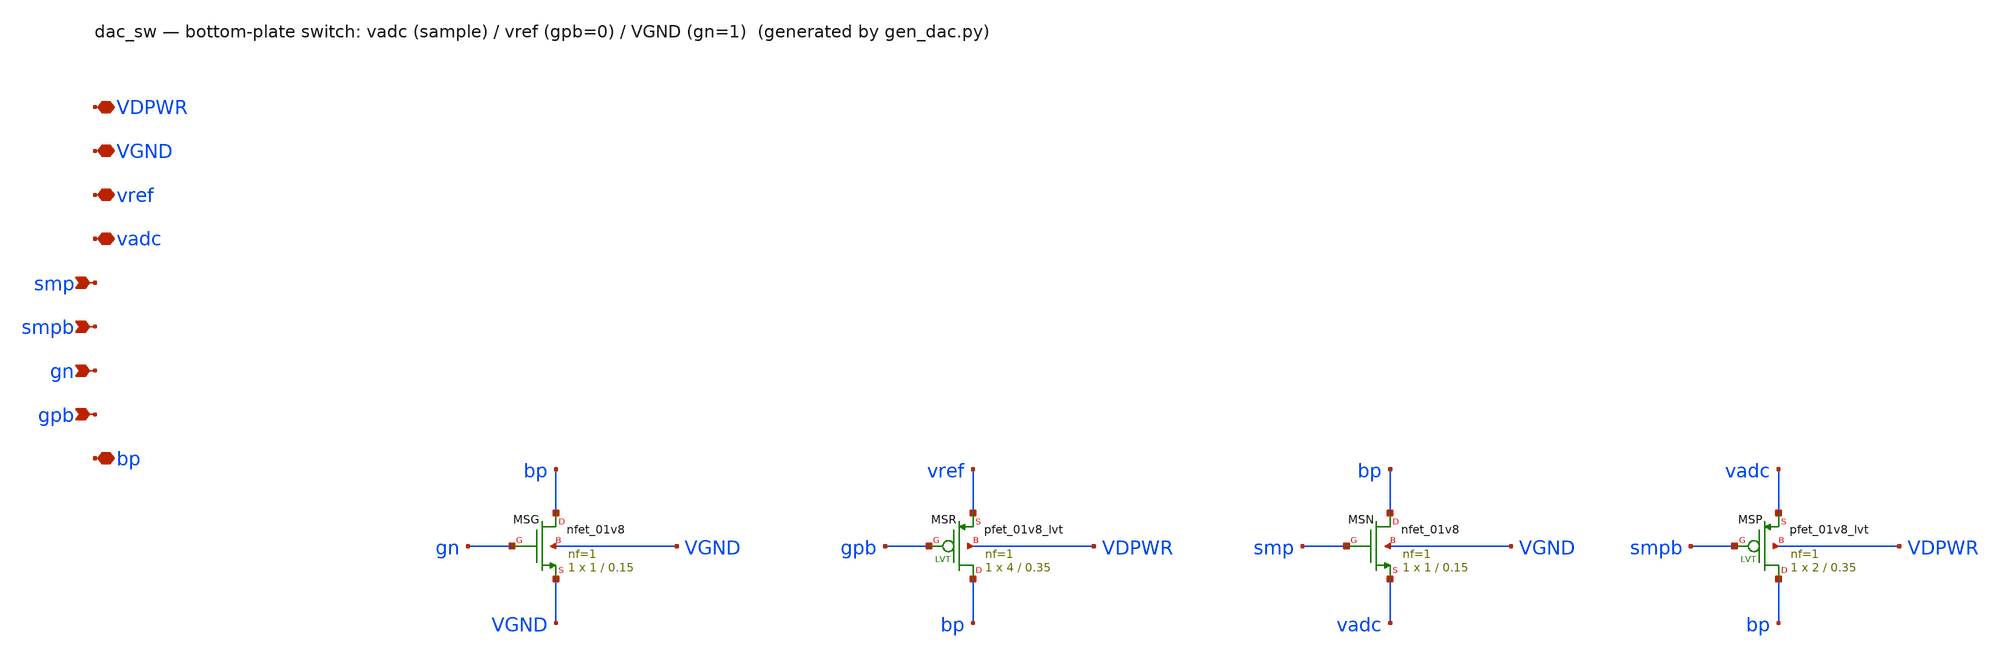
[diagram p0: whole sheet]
** sch_path: xschem/dac_sw.sch
**.subckt dac_sw VDPWR VGND vref vadc smp smpb gn gpb bp
*.iopin VDPWR
*.iopin VGND
*.iopin vref
*.iopin vadc
*.ipin smp
*.ipin smpb
*.ipin gn
*.ipin gpb
*.iopin bp
XMSG bp gn VGND VGND sky130_fd_pr__nfet_01v8 L=0.15 W=1 nf=1 ad='int((1 + 1)/2) * 1 / 1 * 0.29' as='int((1 + 2)/2) * 1 / 1 * 0.29'
+ pd='2*int((1 + 1)/2) * (1 / 1 + 0.29)' ps='2*int((1 + 2)/2) * (1 / 1 + 0.29)' nrd='0.29 / 1 ' nrs='0.29 / 1 '
+ sa=0 sb=0 sd=0 mult=1 m=1
XMSR bp gpb vref VDPWR sky130_fd_pr__pfet_01v8_lvt L=0.35 W=4 nf=1 ad='int((1 + 1)/2) * 4 / 1 * 0.29'
+ as='int((1 + 2)/2) * 4 / 1 * 0.29' pd='2*int((1 + 1)/2) * (4 / 1 + 0.29)' ps='2*int((1 + 2)/2) * (4 / 1 + 0.29)'
+ nrd='0.29 / 4 ' nrs='0.29 / 4 ' sa=0 sb=0 sd=0 mult=1 m=1
XMSN bp smp vadc VGND sky130_fd_pr__nfet_01v8 L=0.15 W=1 nf=1 ad='int((1 + 1)/2) * 1 / 1 * 0.29' as='int((1 + 2)/2) * 1 / 1 * 0.29'
+ pd='2*int((1 + 1)/2) * (1 / 1 + 0.29)' ps='2*int((1 + 2)/2) * (1 / 1 + 0.29)' nrd='0.29 / 1 ' nrs='0.29 / 1 '
+ sa=0 sb=0 sd=0 mult=1 m=1
XMSP bp smpb vadc VDPWR sky130_fd_pr__pfet_01v8_lvt L=0.35 W=2 nf=1 ad='int((1 + 1)/2) * 2 / 1 * 0.29'
+ as='int((1 + 2)/2) * 2 / 1 * 0.29' pd='2*int((1 + 1)/2) * (2 / 1 + 0.29)' ps='2*int((1 + 2)/2) * (2 / 1 + 0.29)'
+ nrd='0.29 / 2 ' nrs='0.29 / 2 ' sa=0 sb=0 sd=0 mult=1 m=1
**.ends
.end
